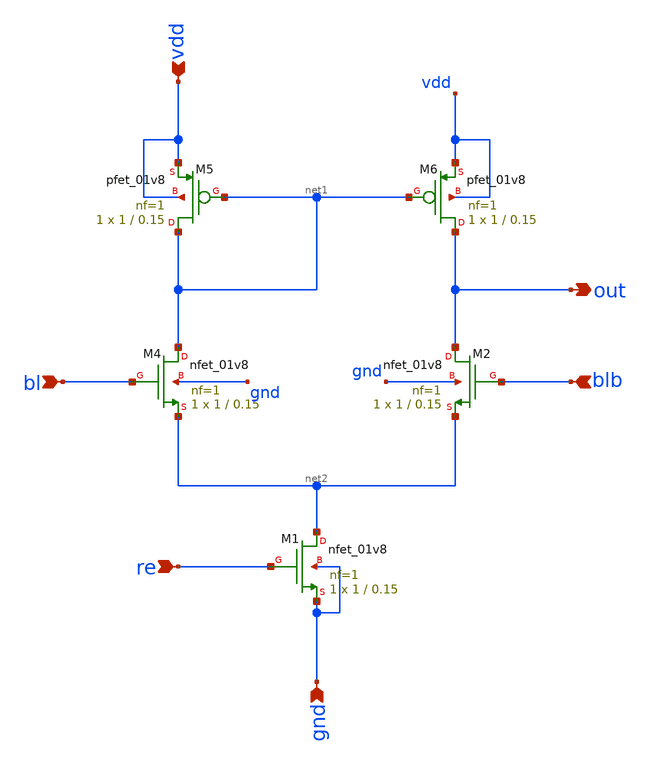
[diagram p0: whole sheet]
** sch_path: sram/sense_amp_2.sch
**.subckt sense_amp_2 gnd vdd re bl blb out
*.ipin gnd
*.ipin vdd
*.ipin re
*.ipin bl
*.ipin blb
*.opin out
XM5 net1 net1 vdd vdd sky130_fd_pr__pfet_01v8 L=0.15 W=1 nf=1 ad='int((nf+1)/2) * W/nf * 0.29' as='int((nf+2)/2) * W/nf * 0.29'
+ pd='2*int((nf+1)/2) * (W/nf + 0.29)' ps='2*int((nf+2)/2) * (W/nf + 0.29)' nrd='0.29 / W' nrs='0.29 / W'
+ sa=0 sb=0 sd=0 mult=1 m=1
XM6 out net1 vdd vdd sky130_fd_pr__pfet_01v8 L=0.15 W=1 nf=1 ad='int((nf+1)/2) * W/nf * 0.29' as='int((nf+2)/2) * W/nf * 0.29'
+ pd='2*int((nf+1)/2) * (W/nf + 0.29)' ps='2*int((nf+2)/2) * (W/nf + 0.29)' nrd='0.29 / W' nrs='0.29 / W'
+ sa=0 sb=0 sd=0 mult=1 m=1
XM2 out blb net2 gnd sky130_fd_pr__nfet_01v8 L=0.15 W=1 nf=1 ad='int((nf+1)/2) * W/nf * 0.29' as='int((nf+2)/2) * W/nf * 0.29'
+ pd='2*int((nf+1)/2) * (W/nf + 0.29)' ps='2*int((nf+2)/2) * (W/nf + 0.29)' nrd='0.29 / W' nrs='0.29 / W'
+ sa=0 sb=0 sd=0 mult=1 m=1
XM4 net1 bl net2 gnd sky130_fd_pr__nfet_01v8 L=0.15 W=1 nf=1 ad='int((nf+1)/2) * W/nf * 0.29' as='int((nf+2)/2) * W/nf * 0.29'
+ pd='2*int((nf+1)/2) * (W/nf + 0.29)' ps='2*int((nf+2)/2) * (W/nf + 0.29)' nrd='0.29 / W' nrs='0.29 / W'
+ sa=0 sb=0 sd=0 mult=1 m=1
XM1 net2 re gnd gnd sky130_fd_pr__nfet_01v8 L=0.15 W=1 nf=1 ad='int((nf+1)/2) * W/nf * 0.29' as='int((nf+2)/2) * W/nf * 0.29'
+ pd='2*int((nf+1)/2) * (W/nf + 0.29)' ps='2*int((nf+2)/2) * (W/nf + 0.29)' nrd='0.29 / W' nrs='0.29 / W'
+ sa=0 sb=0 sd=0 mult=1 m=1
**.ends
.end
